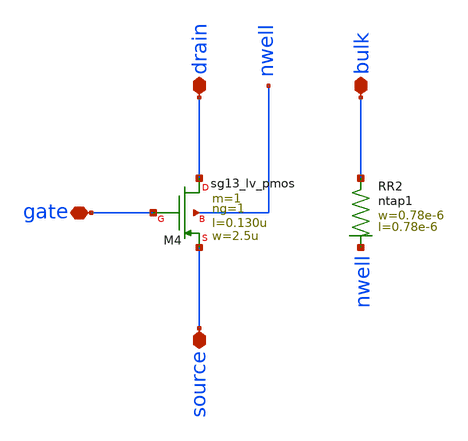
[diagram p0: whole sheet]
** sch_path: ts_pr_May2024/design_data/xschem/pmos1.sch
**.subckt pmos1 gate drain source bulk
*.iopin gate
*.iopin drain
*.iopin source
*.iopin bulk
XR2 bulk nwell ntap1 R=262.8 w=0.78e-6 l=0.78e-6
XM4 drain gate source nwell sg13_lv_pmos w=2.5u l=0.130u ng=1 m=1 mm_ok=1
**.ends
.end
